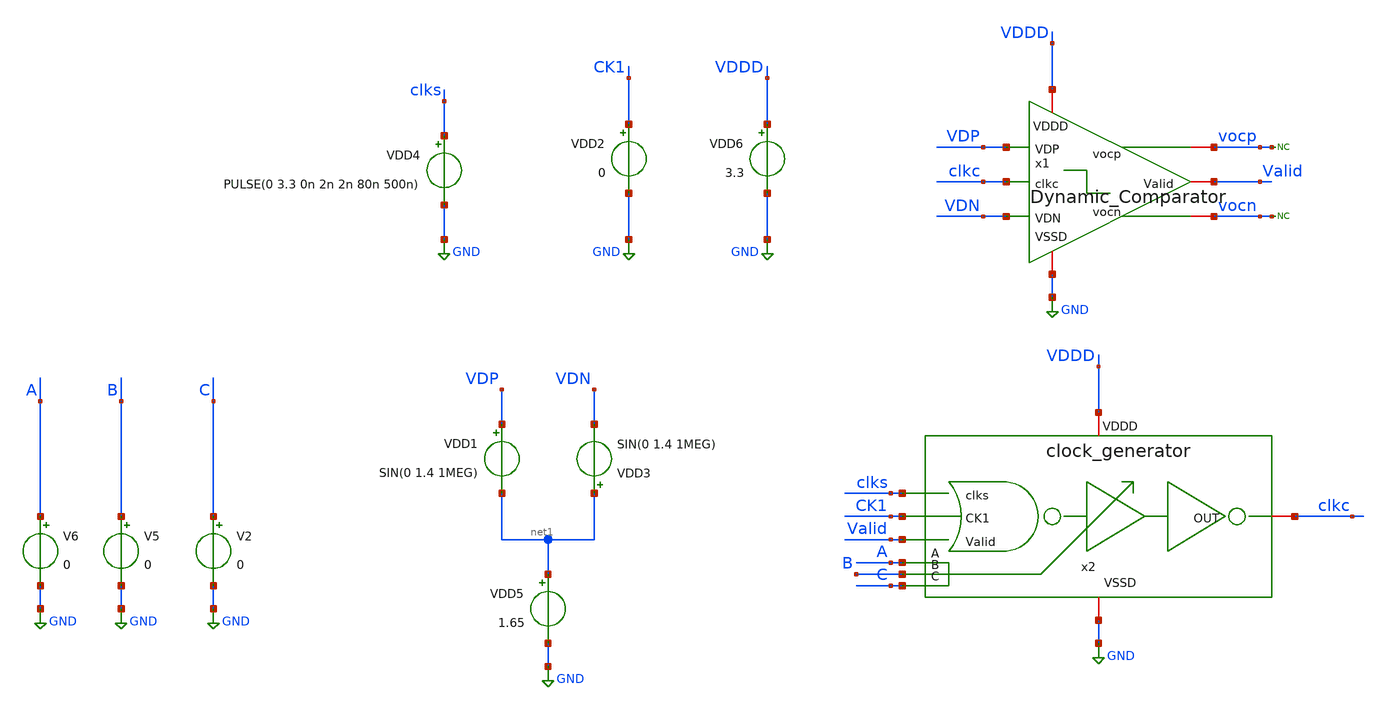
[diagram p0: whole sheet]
** sch_path: SAR_ADC/Dynamic_Comparator/xschem/Dynamic_Comparator_Clock_generator_tb.sch
**.subckt Dynamic_Comparator_Clock_generator_tb
VDD6 VDDD GND 3.3
VDD1 VDP net1 SIN(0 1.4 1MEG)
VDD3 net1 VDN SIN(0 1.4 1MEG)
VDD5 net1 GND 1.65
VDD2 CK1 GND 0
VDD4 clks GND PULSE(0 3.3 0n 2n 2n 80n 500n)
* noconn vocp
* noconn vocn
V2 C GND 0
V5 B GND 0
V6 A GND 0
x1 vocp vocn VDDD GND VDP VDN Valid clkc Dynamic_Comparator
x2 clkc VDDD GND clks CK1 Valid A B C clock_generator
**** begin user architecture code



*Parameters

.options TEMP = 50.0
.lib /home/gf180/Documents/gf180/pdk/gf180mcuD/libs.tech/ngspice/sm141064.ngspice typical
.lib /home/gf180/Documents/gf180/pdk/gf180mcuD/libs.tech/ngspice/sm141064.ngspice cap_mim

.lib /home/gf180/Documents/gf180/pdk/gf180mcuD/libs.tech/ngspice/sm141064.ngspice mimcap_statistical
.include /home/gf180/Documents/gf180/pdk/gf180mcuD/libs.tech/ngspice/design.ngspice

*Data to save
.save v(VDP)
.save v(VDN)
.save v(clkc)
.save v(clks)
.save v(Valid)
.save v(vocp)
.save v(vocn)
.save v(CK1)

* Simulation
.control
tran 0.1n 1u 0.01n
setplot dc1
plot v(clks)+12 v(CK1)+8 v(Valid)+4 v(clkc)
set filetype = ascii
write Dynamic_Comparator_Clock_generator_tb_tran.raw

reset
unset filetype
op
save all
write Dynamic_Comparator_Clock_generator_tb.raw


.endc
.end


**** end user architecture code
**.ends
.GLOBAL GND
.end
